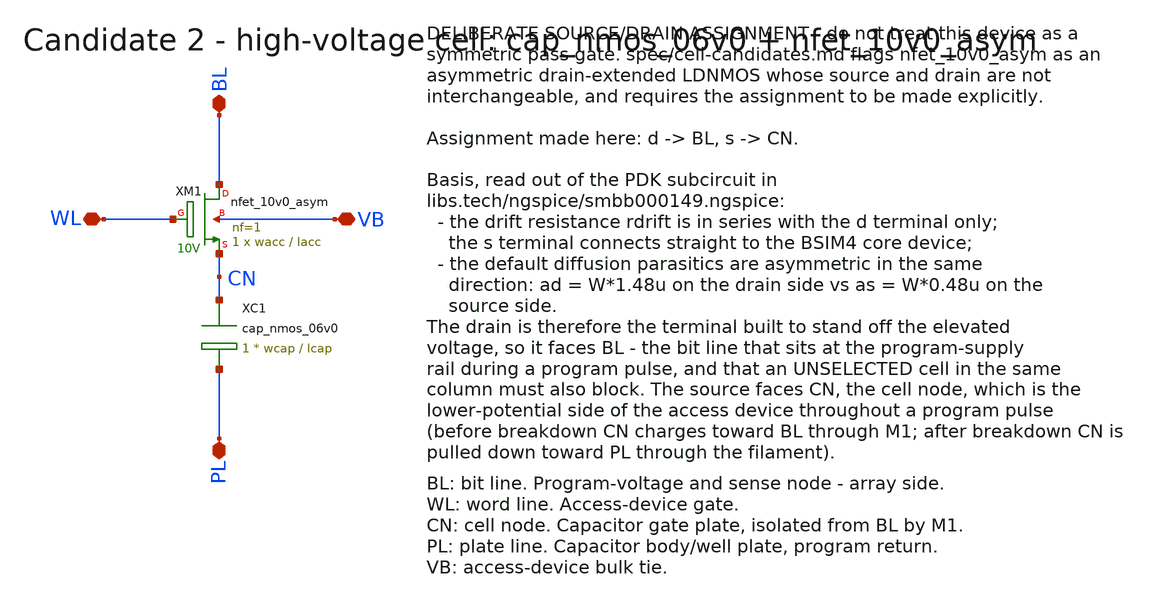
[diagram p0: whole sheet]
** sch_path: design/cells/cell_candidate2.sch
**.subckt cell_candidate2 BL WL PL VB
*.iopin BL
*.iopin WL
*.iopin PL
*.iopin VB
XM1 BL WL CN VB nfet_10v0_asym L=lacc W=wacc nf=1 ad='wacc * 1.48u' as='wacc * 0.48u' pd='2 * (wacc + 1.48u)'
+ ps='2 * (wacc + 0.48u)' nrd=0 nrs=0 sa=0 sb=0 sd=0 m=1
XC1 CN PL cap_nmos_06v0 c_width=wcap c_length=lcap m=1
**.ends
.end
